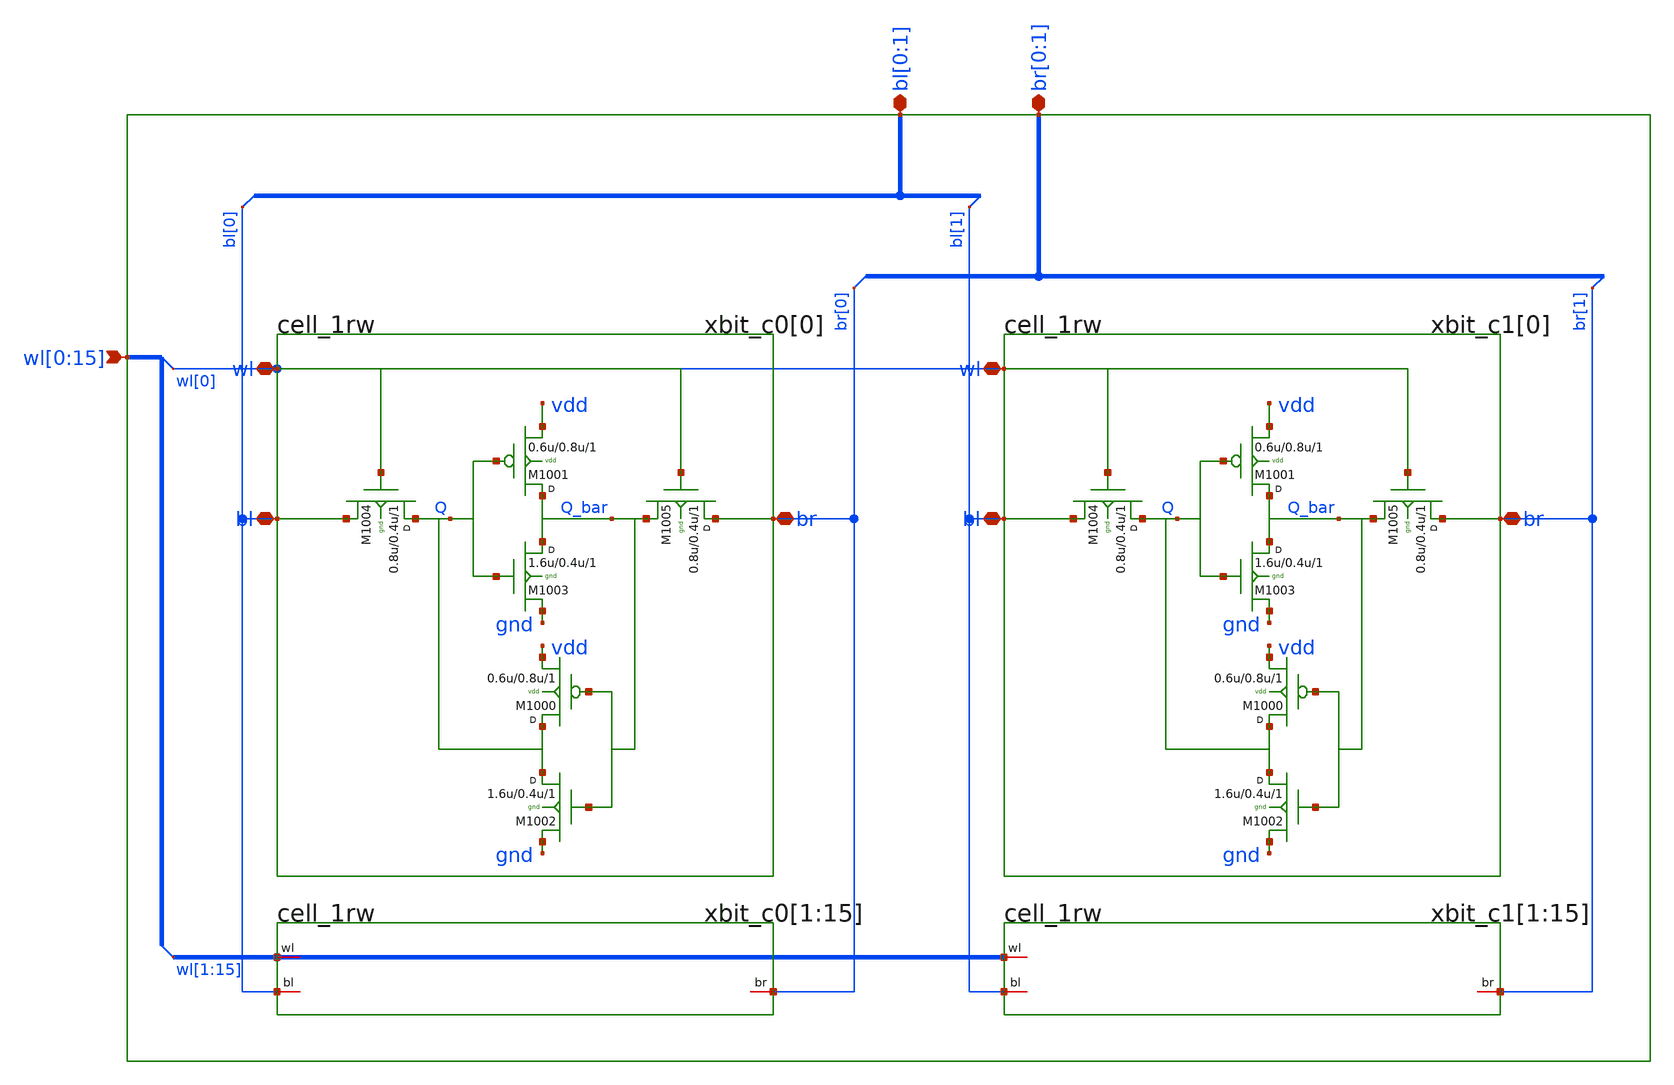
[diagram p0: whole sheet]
** sch_path: sram_2_16_scn4m/bitcell_array.sch
**.subckt bitcell_array bl[0],bl[1]
*+ wl[0],wl[1],wl[2],wl[3],wl[4],wl[5],wl[6],wl[7],wl[8],wl[9],wl[10],wl[11],wl[12],wl[13],wl[14],wl[15] br[0],br[1]
*.iopin bl[0],bl[1]
*.ipin
*+ wl[0],wl[1],wl[2],wl[3],wl[4],wl[5],wl[6],wl[7],wl[8],wl[9],wl[10],wl[11],wl[12],wl[13],wl[14],wl[15]
*.iopin br[0],br[1]
xbit_c0[1] bl[0] br[0] wl[1] vdd gnd cell_1rw
xbit_c0[2] bl[0] br[0] wl[2] vdd gnd cell_1rw
xbit_c0[3] bl[0] br[0] wl[3] vdd gnd cell_1rw
xbit_c0[4] bl[0] br[0] wl[4] vdd gnd cell_1rw
xbit_c0[5] bl[0] br[0] wl[5] vdd gnd cell_1rw
xbit_c0[6] bl[0] br[0] wl[6] vdd gnd cell_1rw
xbit_c0[7] bl[0] br[0] wl[7] vdd gnd cell_1rw
xbit_c0[8] bl[0] br[0] wl[8] vdd gnd cell_1rw
xbit_c0[9] bl[0] br[0] wl[9] vdd gnd cell_1rw
xbit_c0[10] bl[0] br[0] wl[10] vdd gnd cell_1rw
xbit_c0[11] bl[0] br[0] wl[11] vdd gnd cell_1rw
xbit_c0[12] bl[0] br[0] wl[12] vdd gnd cell_1rw
xbit_c0[13] bl[0] br[0] wl[13] vdd gnd cell_1rw
xbit_c0[14] bl[0] br[0] wl[14] vdd gnd cell_1rw
xbit_c0[15] bl[0] br[0] wl[15] vdd gnd cell_1rw
xbit_c0[0] bl[0] br[0] wl[0] vdd gnd cell_1rw
xbit_c1[1] bl[1] br[1] wl[1] vdd gnd cell_1rw
xbit_c1[2] bl[1] br[1] wl[2] vdd gnd cell_1rw
xbit_c1[3] bl[1] br[1] wl[3] vdd gnd cell_1rw
xbit_c1[4] bl[1] br[1] wl[4] vdd gnd cell_1rw
xbit_c1[5] bl[1] br[1] wl[5] vdd gnd cell_1rw
xbit_c1[6] bl[1] br[1] wl[6] vdd gnd cell_1rw
xbit_c1[7] bl[1] br[1] wl[7] vdd gnd cell_1rw
xbit_c1[8] bl[1] br[1] wl[8] vdd gnd cell_1rw
xbit_c1[9] bl[1] br[1] wl[9] vdd gnd cell_1rw
xbit_c1[10] bl[1] br[1] wl[10] vdd gnd cell_1rw
xbit_c1[11] bl[1] br[1] wl[11] vdd gnd cell_1rw
xbit_c1[12] bl[1] br[1] wl[12] vdd gnd cell_1rw
xbit_c1[13] bl[1] br[1] wl[13] vdd gnd cell_1rw
xbit_c1[14] bl[1] br[1] wl[14] vdd gnd cell_1rw
xbit_c1[15] bl[1] br[1] wl[15] vdd gnd cell_1rw
xbit_c1[0] bl[1] br[1] wl[0] vdd gnd cell_1rw
**.ends

* expanding   symbol:  cell_1rw.sym # of pins=3
** sym_path: sram_2_16_scn4m/cell_1rw.sym
** sch_path: sram_2_16_scn4m/cell_1rw.sch
.subckt cell_1rw bl br wl vdd gnd
*.iopin bl
*.iopin br
*.iopin wl
M1004 Q wl bl gnd n w=0.8u l=0.4u m=1
M1001 Q_bar Q vdd vdd p w=0.6u l=0.8u m=1
M1003 Q_bar Q gnd gnd n w=1.6u l=0.4u m=1
M1002 Q Q_bar gnd gnd n w=1.6u l=0.4u m=1
M1000 Q Q_bar vdd vdd p w=0.6u l=0.8u m=1
M1005 br wl Q_bar gnd n w=0.8u l=0.4u m=1
.ends

.end
